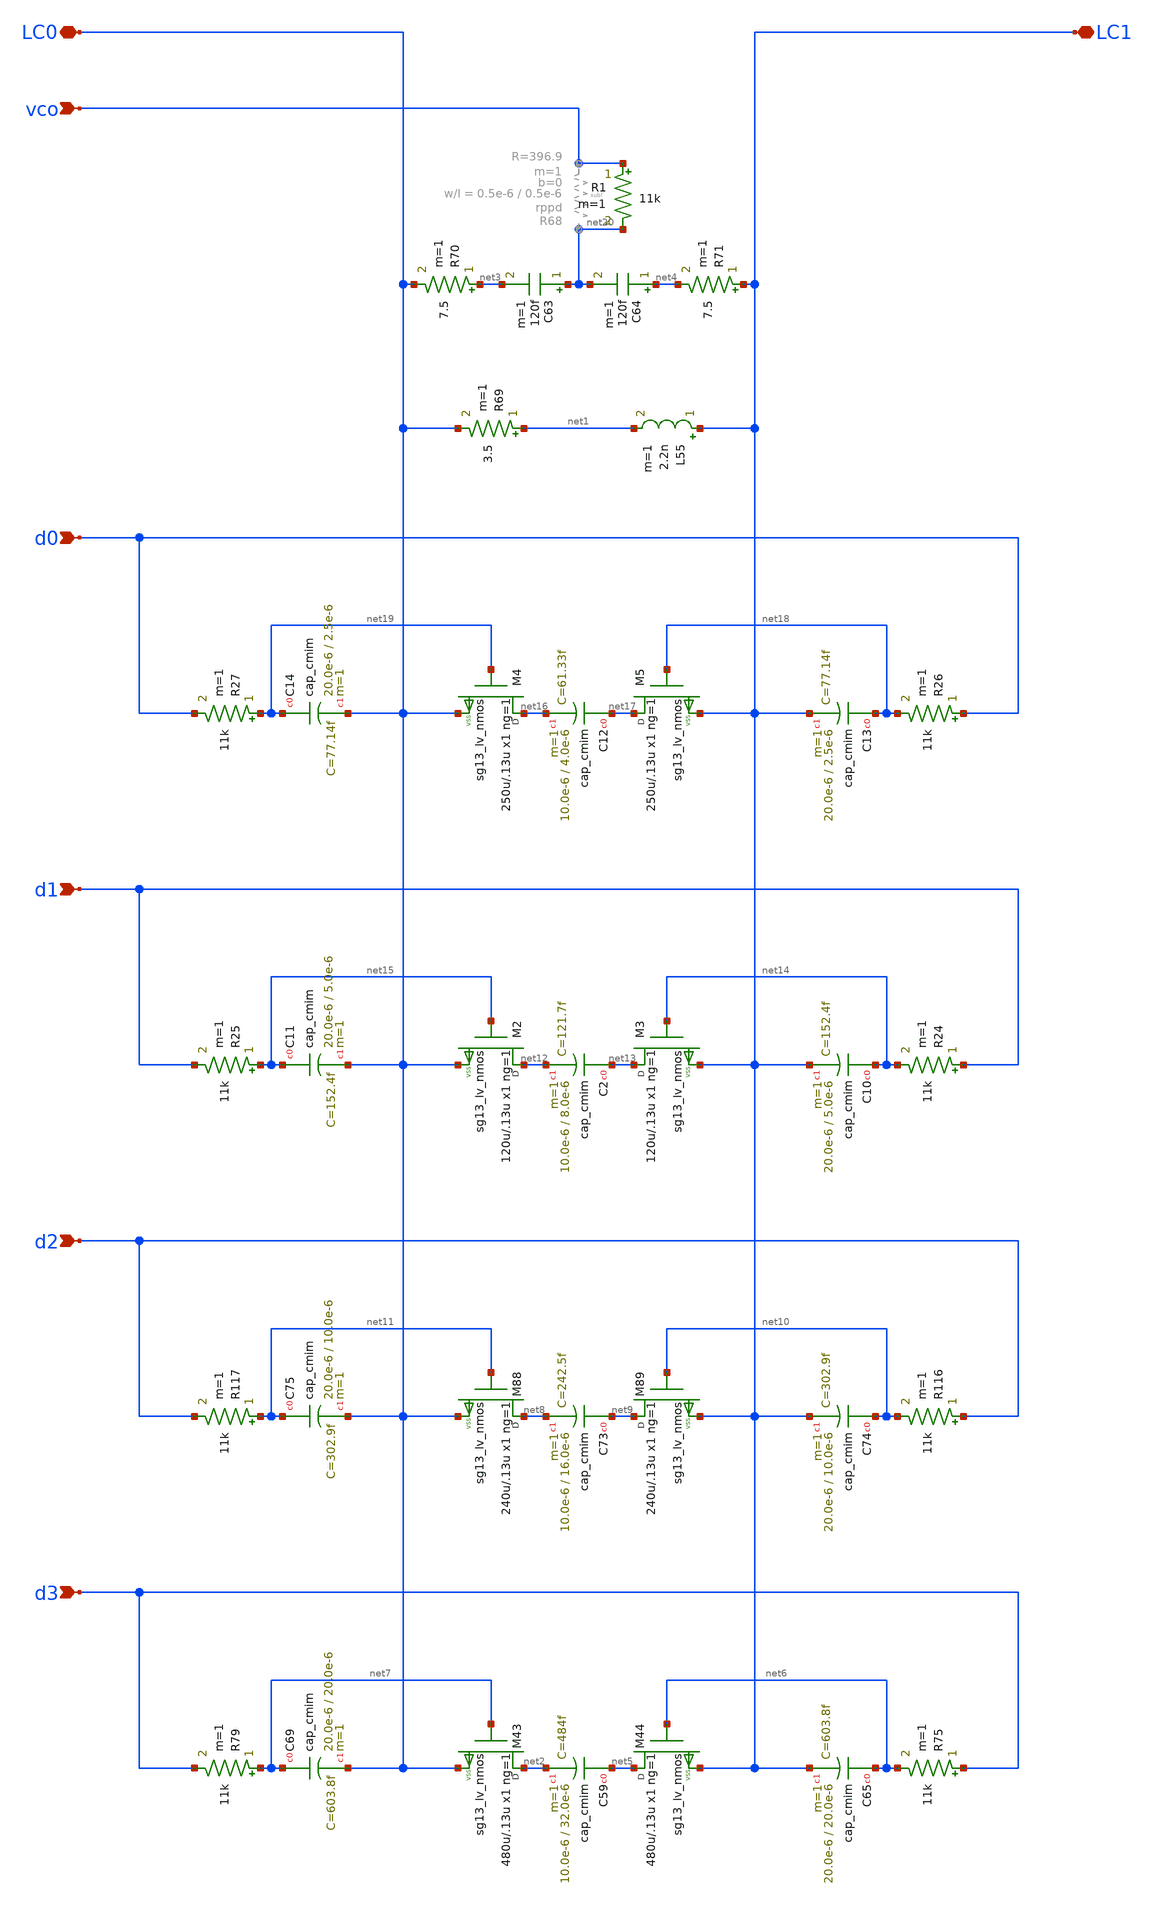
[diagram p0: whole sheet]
** sch_path: design_data/xschem/LC_tank_01.sch
* Copyright (C) 1998-2023 Stefan Frederik Schippers
* This program is free software; you can redistribute it and/or modify
* it under the terms of the GNU General Public License as published by
* the Free Software Foundation; either version 2 of the License, or
* (at your option) any later version.
* This program is distributed in the hope that it will be useful,
* but WITHOUT ANY WARRANTY; without even the implied warranty of
* MERCHANTABILITY or FITNESS FOR A PARTICULAR PURPOSE.  See the
* GNU General Public License for more details.
* You should have received a copy of the GNU General Public License
* along with this program; if not, write to the Free Software
**.subckt LC_tank_01 LC0 LC1 d0 d1 d2 d3 vco
*.iopin LC0
*.iopin LC1
*.ipin d0
*.ipin d1
*.ipin d2
*.ipin d3
*.ipin vco
L55 LC1 net1 2.2n m=1
R69 net1 LC0 3.5 m=1
XC59 net5 net2 cap_cmim w=10.0e-6 l=32.0e-6 m=1 mm_ok=1
R70 net3 LC0 7.5 m=1
C63 net20 net3 120f m=1
C64 net4 net20 120f m=1
R71 LC1 net4 7.5 m=1
XM43 net2 net7 LC0 VSS sg13_lv_nmos w=480u l=.13u ng=1 m=1
XM44 net5 net6 LC1 VSS sg13_lv_nmos w=480u l=.13u ng=1 m=1
XC65 net6 LC1 cap_cmim w=20.0e-6 l=20.0e-6 m=1 mm_ok=1
R75 d3 net6 11k m=1
XC69 net7 LC0 cap_cmim w=20.0e-6 l=20.0e-6 m=1 mm_ok=1
R79 net7 d3 11k m=1
XC73 net9 net8 cap_cmim w=10.0e-6 l=16.0e-6 m=1 mm_ok=1
XM88 net8 net11 LC0 VSS sg13_lv_nmos w=240u l=.13u ng=1 m=1
XM89 net9 net10 LC1 VSS sg13_lv_nmos w=240u l=.13u ng=1 m=1
XC74 net10 LC1 cap_cmim w=20.0e-6 l=10.0e-6 m=1 mm_ok=1
R116 d2 net10 11k m=1
XC75 net11 LC0 cap_cmim w=20.0e-6 l=10.0e-6 m=1 mm_ok=1
R117 net11 d2 11k m=1
XC2 net13 net12 cap_cmim w=10.0e-6 l=8.0e-6 m=1 mm_ok=1
XM2 net12 net15 LC0 VSS sg13_lv_nmos w=120u l=.13u ng=1 m=1
XM3 net13 net14 LC1 VSS sg13_lv_nmos w=120u l=.13u ng=1 m=1
XC10 net14 LC1 cap_cmim w=20.0e-6 l=5.0e-6 m=1 mm_ok=1
R24 d1 net14 11k m=1
XC11 net15 LC0 cap_cmim w=20.0e-6 l=5.0e-6 m=1 mm_ok=1
R25 net15 d1 11k m=1
XC12 net17 net16 cap_cmim w=10.0e-6 l=4.0e-6 m=1 mm_ok=1
XM4 net16 net19 LC0 VSS sg13_lv_nmos w=250u l=.13u ng=1 m=1
XM5 net17 net18 LC1 VSS sg13_lv_nmos w=250u l=.13u ng=1 m=1
XC13 net18 LC1 cap_cmim w=20.0e-6 l=2.5e-6 m=1 mm_ok=1
R26 d0 net18 11k m=1
XC14 net19 LC0 cap_cmim w=20.0e-6 l=2.5e-6 m=1 mm_ok=1
R27 net19 d0 11k m=1
R1 vco net20 11k m=1
**.ends
.end
